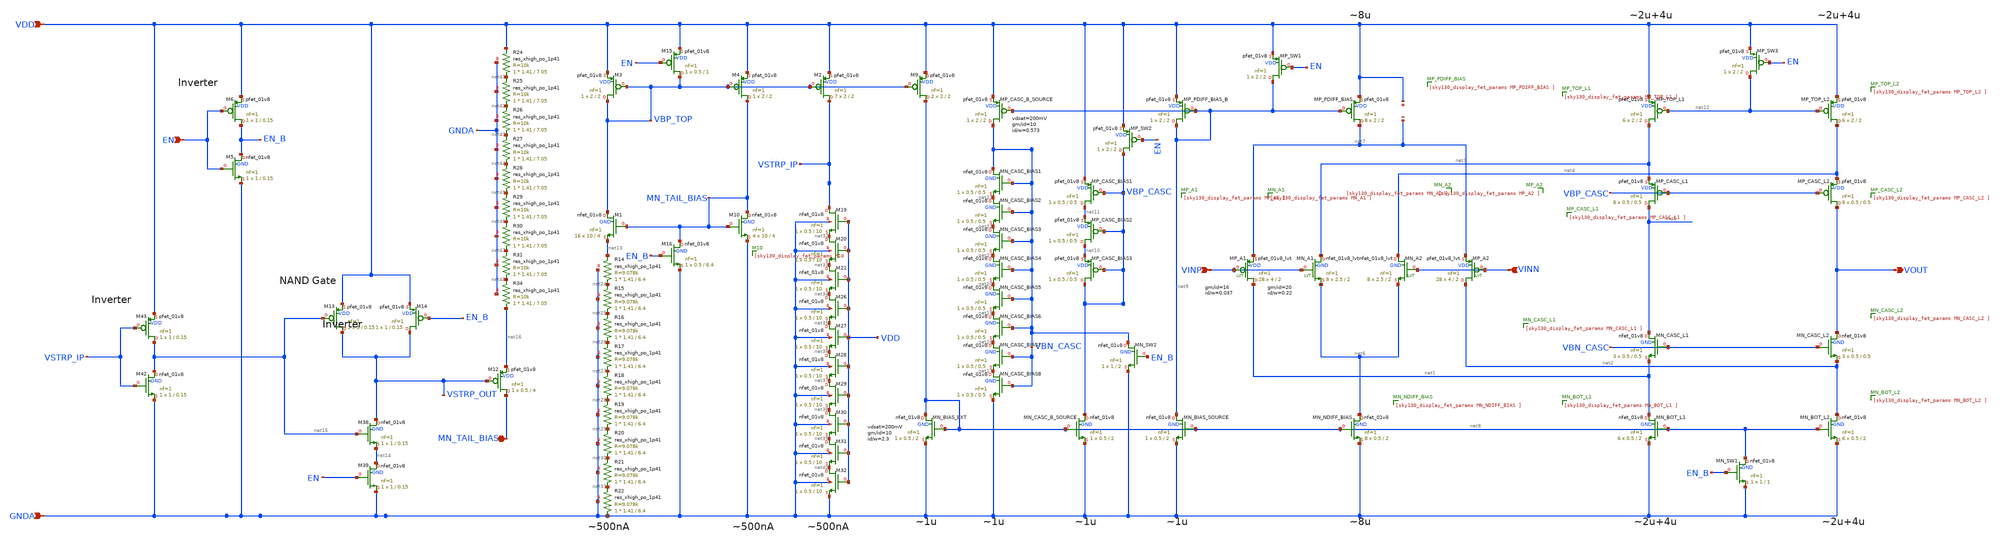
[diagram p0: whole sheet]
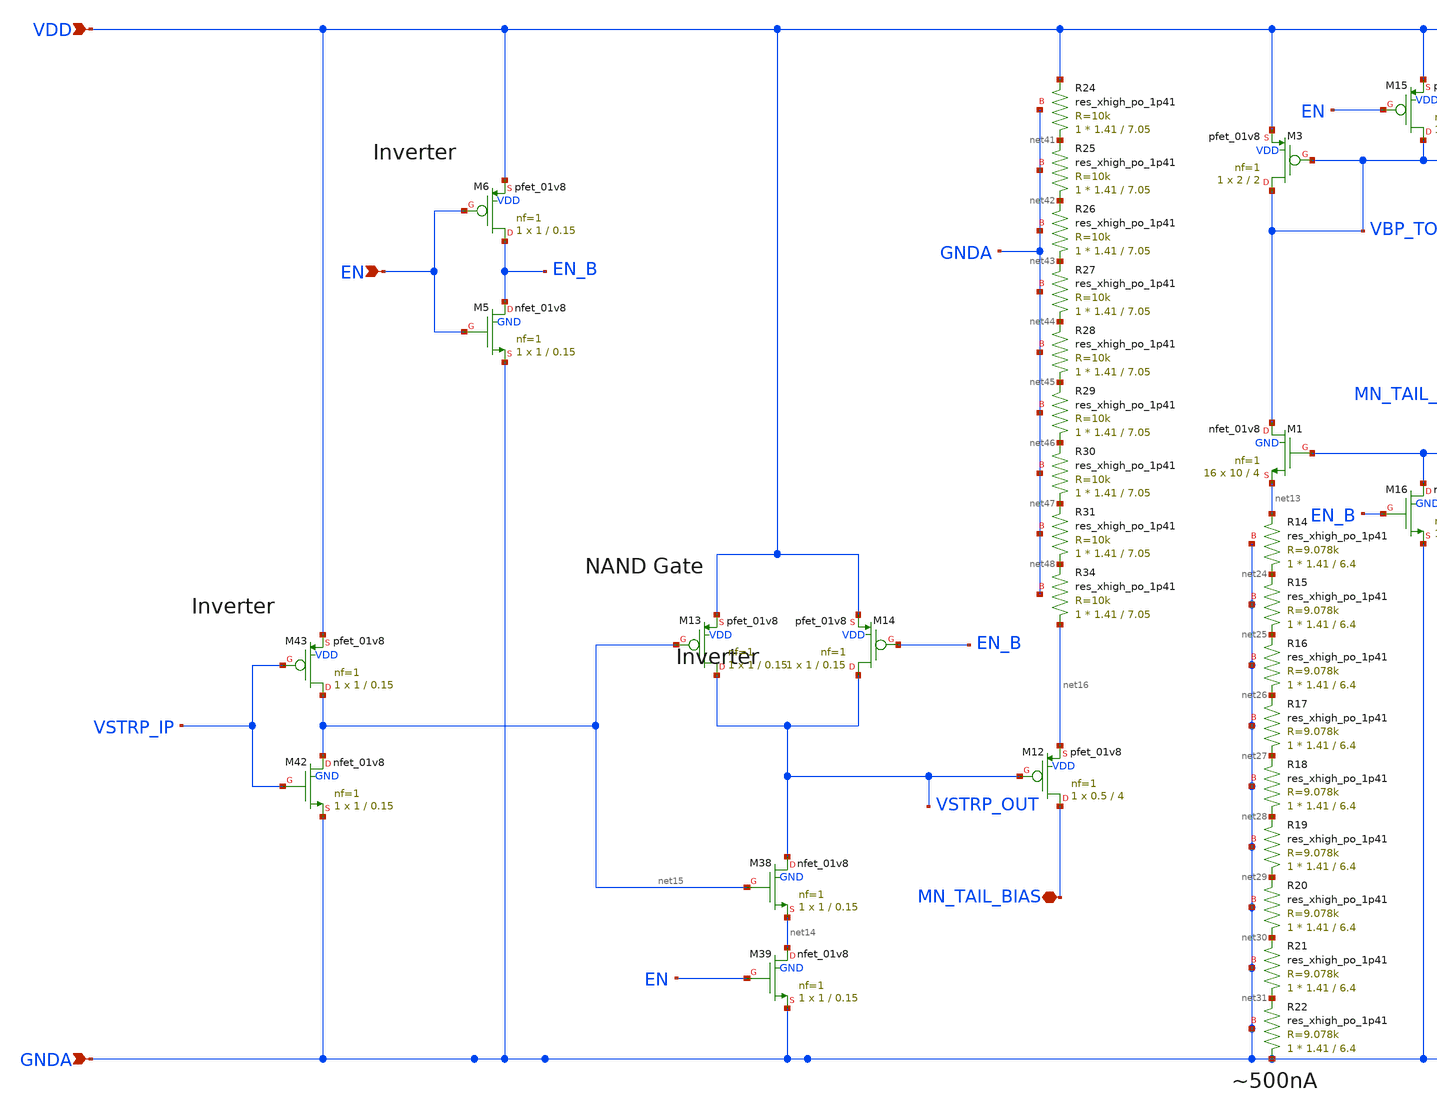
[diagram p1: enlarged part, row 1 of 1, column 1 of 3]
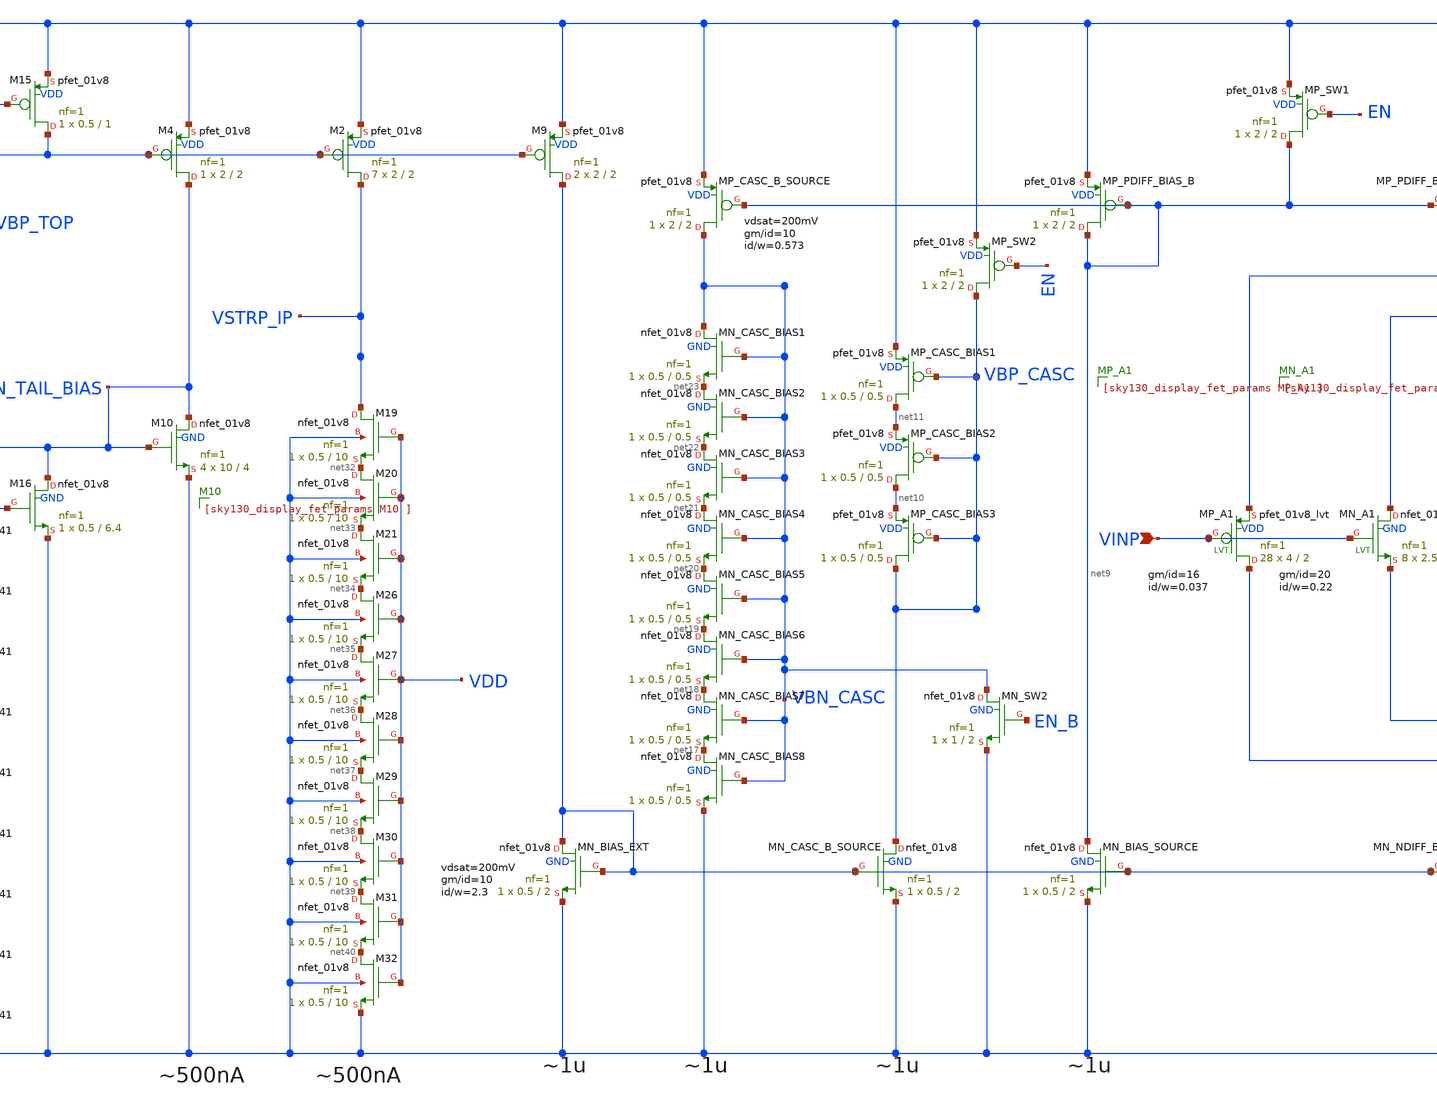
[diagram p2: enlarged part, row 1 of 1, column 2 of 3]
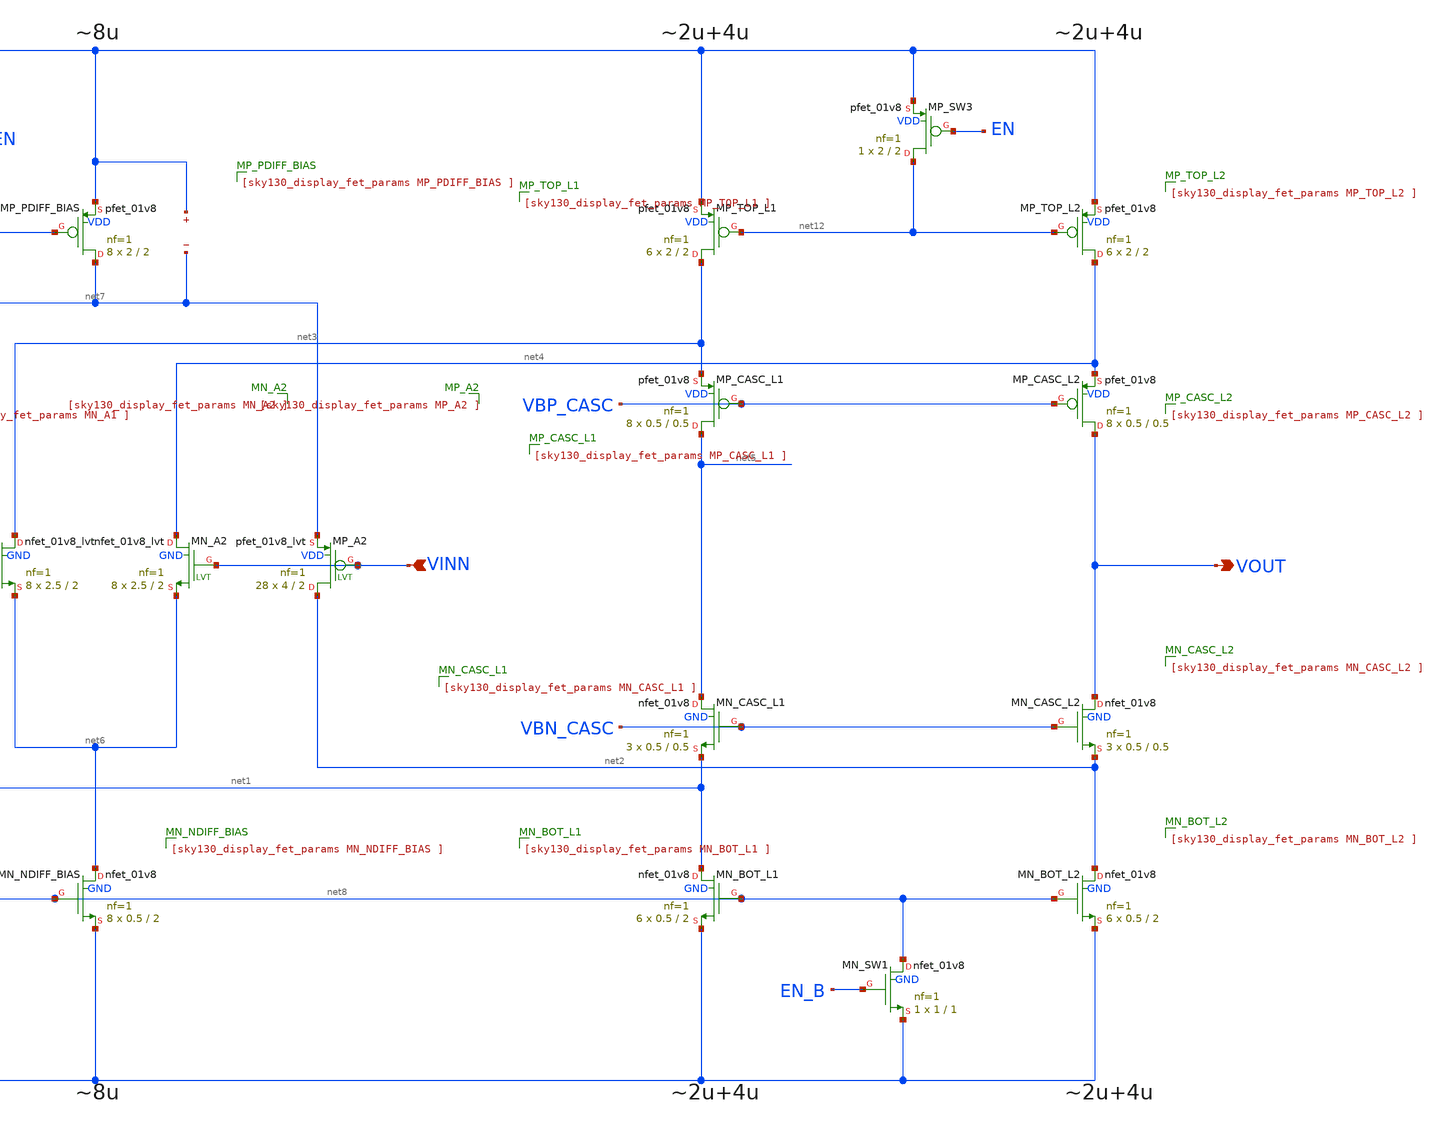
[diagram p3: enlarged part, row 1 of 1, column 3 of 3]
** sch_path: OTAs/Rail_to_Rail_OTA_Inp_IP/fully_differential/Rail_to_Rail_IP_OTA_Fully_Diff_with_Internal_bias.sch
**.subckt Rail_to_Rail_IP_OTA_Fully_Diff_with_Internal_bias VINP VINN VDD GNDA VOUT EN MN_TAIL_BIAS
*.ipin VINP
*.ipin VINN
*.ipin VDD
*.ipin GNDA
*.opin VOUT
*.ipin EN
*.iopin MN_TAIL_BIAS
XMN_BOT_L2 net2 net8 GNDA GND sky130_fd_pr__nfet_01v8 L=2 W=0.5 nf=1 ad='int((1 + 1)/2) * 0.5 / 1 * 0.29'
+ as='int((1 + 2)/2) * 0.5 / 1 * 0.29' pd='2*int((1 + 1)/2) * (0.5 / 1 + 0.29)' ps='2*int((1 + 2)/2) * (0.5 / 1 + 0.29)'
+ nrd='0.29 / 0.5 ' nrs='0.29 / 0.5 ' sa=0 sb=0 sd=0 mult=6 m=6
XMN_CASC_L2 VOUT VBN_CASC net2 GND sky130_fd_pr__nfet_01v8 L=0.5 W=0.5 nf=1 ad='int((1 + 1)/2) * 0.5 / 1 * 0.29'
+ as='int((1 + 2)/2) * 0.5 / 1 * 0.29' pd='2*int((1 + 1)/2) * (0.5 / 1 + 0.29)' ps='2*int((1 + 2)/2) * (0.5 / 1 + 0.29)'
+ nrd='0.29 / 0.5 ' nrs='0.29 / 0.5 ' sa=0 sb=0 sd=0 mult=3 m=3
XMN_BOT_L1 net1 net8 GNDA GND sky130_fd_pr__nfet_01v8 L=2 W=0.5 nf=1 ad='int((1 + 1)/2) * 0.5 / 1 * 0.29'
+ as='int((1 + 2)/2) * 0.5 / 1 * 0.29' pd='2*int((1 + 1)/2) * (0.5 / 1 + 0.29)' ps='2*int((1 + 2)/2) * (0.5 / 1 + 0.29)'
+ nrd='0.29 / 0.5 ' nrs='0.29 / 0.5 ' sa=0 sb=0 sd=0 mult=6 m=6
XMN_CASC_L1 net5 VBN_CASC net1 GND sky130_fd_pr__nfet_01v8 L=0.5 W=0.5 nf=1 ad='int((1 + 1)/2) * 0.5 / 1 * 0.29'
+ as='int((1 + 2)/2) * 0.5 / 1 * 0.29' pd='2*int((1 + 1)/2) * (0.5 / 1 + 0.29)' ps='2*int((1 + 2)/2) * (0.5 / 1 + 0.29)'
+ nrd='0.29 / 0.5 ' nrs='0.29 / 0.5 ' sa=0 sb=0 sd=0 mult=3 m=3
XMP_CASC_L2 VOUT VBP_CASC net4 VDD sky130_fd_pr__pfet_01v8 L=0.5 W=0.5 nf=1 ad='int((1 + 1)/2) * 0.5 / 1 * 0.29'
+ as='int((1 + 2)/2) * 0.5 / 1 * 0.29' pd='2*int((1 + 1)/2) * (0.5 / 1 + 0.29)' ps='2*int((1 + 2)/2) * (0.5 / 1 + 0.29)'
+ nrd='0.29 / 0.5 ' nrs='0.29 / 0.5 ' sa=0 sb=0 sd=0 mult=8 m=8
XMP_CASC_L1 net5 VBP_CASC net3 VDD sky130_fd_pr__pfet_01v8 L=0.5 W=0.5 nf=1 ad='int((1 + 1)/2) * 0.5 / 1 * 0.29'
+ as='int((1 + 2)/2) * 0.5 / 1 * 0.29' pd='2*int((1 + 1)/2) * (0.5 / 1 + 0.29)' ps='2*int((1 + 2)/2) * (0.5 / 1 + 0.29)'
+ nrd='0.29 / 0.5 ' nrs='0.29 / 0.5 ' sa=0 sb=0 sd=0 mult=8 m=8
XMP_TOP_L1 net3 net12 VDD VDD sky130_fd_pr__pfet_01v8 L=2 W=2 nf=1 ad='int((1 + 1)/2) * 2 / 1 * 0.29'
+ as='int((1 + 2)/2) * 2 / 1 * 0.29' pd='2*int((1 + 1)/2) * (2 / 1 + 0.29)' ps='2*int((1 + 2)/2) * (2 / 1 + 0.29)'
+ nrd='0.29 / 2 ' nrs='0.29 / 2 ' sa=0 sb=0 sd=0 mult=6 m=6
XMN_A1 net3 VINP net6 GND sky130_fd_pr__nfet_01v8_lvt L=2 W=2.5 nf=1 ad='int((1 + 1)/2) * 2.5 / 1 * 0.29'
+ as='int((1 + 2)/2) * 2.5 / 1 * 0.29' pd='2*int((1 + 1)/2) * (2.5 / 1 + 0.29)' ps='2*int((1 + 2)/2) * (2.5 / 1 + 0.29)'
+ nrd='0.29 / 2.5 ' nrs='0.29 / 2.5 ' sa=0 sb=0 sd=0 mult=8 m=8
XMN_A2 net4 VINN net6 GND sky130_fd_pr__nfet_01v8_lvt L=2 W=2.5 nf=1 ad='int((1 + 1)/2) * 2.5 / 1 * 0.29'
+ as='int((1 + 2)/2) * 2.5 / 1 * 0.29' pd='2*int((1 + 1)/2) * (2.5 / 1 + 0.29)' ps='2*int((1 + 2)/2) * (2.5 / 1 + 0.29)'
+ nrd='0.29 / 2.5 ' nrs='0.29 / 2.5 ' sa=0 sb=0 sd=0 mult=8 m=8
XMP_A1 net1 VINP net7 VDD sky130_fd_pr__pfet_01v8_lvt L=2 W=4 nf=1 ad='int((1 + 1)/2) * 4 / 1 * 0.29'
+ as='int((1 + 2)/2) * 4 / 1 * 0.29' pd='2*int((1 + 1)/2) * (4 / 1 + 0.29)' ps='2*int((1 + 2)/2) * (4 / 1 + 0.29)'
+ nrd='0.29 / 4 ' nrs='0.29 / 4 ' sa=0 sb=0 sd=0 mult=28 m=28
XMP_A2 net2 VINN net7 VDD sky130_fd_pr__pfet_01v8_lvt L=2 W=4 nf=1 ad='int((1 + 1)/2) * 4 / 1 * 0.29'
+ as='int((1 + 2)/2) * 4 / 1 * 0.29' pd='2*int((1 + 1)/2) * (4 / 1 + 0.29)' ps='2*int((1 + 2)/2) * (4 / 1 + 0.29)'
+ nrd='0.29 / 4 ' nrs='0.29 / 4 ' sa=0 sb=0 sd=0 mult=28 m=28
XMP_PDIFF_BIAS net7 net9 VDD VDD sky130_fd_pr__pfet_01v8 L=2 W=2 nf=1 ad='int((1 + 1)/2) * 2 / 1 * 0.29'
+ as='int((1 + 2)/2) * 2 / 1 * 0.29' pd='2*int((1 + 1)/2) * (2 / 1 + 0.29)' ps='2*int((1 + 2)/2) * (2 / 1 + 0.29)'
+ nrd='0.29 / 2 ' nrs='0.29 / 2 ' sa=0 sb=0 sd=0 mult=8 m=8
XMN_NDIFF_BIAS net6 net8 GNDA GND sky130_fd_pr__nfet_01v8 L=2 W=0.5 nf=1 ad='int((1 + 1)/2) * 0.5 / 1 * 0.29'
+ as='int((1 + 2)/2) * 0.5 / 1 * 0.29' pd='2*int((1 + 1)/2) * (0.5 / 1 + 0.29)' ps='2*int((1 + 2)/2) * (0.5 / 1 + 0.29)'
+ nrd='0.29 / 0.5 ' nrs='0.29 / 0.5 ' sa=0 sb=0 sd=0 mult=8 m=8
XMP_PDIFF_BIAS_B net9 net9 VDD VDD sky130_fd_pr__pfet_01v8 L=2 W=2 nf=1 ad='int((1 + 1)/2) * 2 / 1 * 0.29'
+ as='int((1 + 2)/2) * 2 / 1 * 0.29' pd='2*int((1 + 1)/2) * (2 / 1 + 0.29)' ps='2*int((1 + 2)/2) * (2 / 1 + 0.29)'
+ nrd='0.29 / 2 ' nrs='0.29 / 2 ' sa=0 sb=0 sd=0 mult=1 m=1
XMP_TOP_L2 net4 net12 VDD VDD sky130_fd_pr__pfet_01v8 L=2 W=2 nf=1 ad='int((1 + 1)/2) * 2 / 1 * 0.29'
+ as='int((1 + 2)/2) * 2 / 1 * 0.29' pd='2*int((1 + 1)/2) * (2 / 1 + 0.29)' ps='2*int((1 + 2)/2) * (2 / 1 + 0.29)'
+ nrd='0.29 / 2 ' nrs='0.29 / 2 ' sa=0 sb=0 sd=0 mult=6 m=6
XMN_BIAS_SOURCE net9 net8 GNDA GND sky130_fd_pr__nfet_01v8 L=2 W=0.5 nf=1 ad='int((1 + 1)/2) * 0.5 / 1 * 0.29'
+ as='int((1 + 2)/2) * 0.5 / 1 * 0.29' pd='2*int((1 + 1)/2) * (0.5 / 1 + 0.29)' ps='2*int((1 + 2)/2) * (0.5 / 1 + 0.29)'
+ nrd='0.29 / 0.5 ' nrs='0.29 / 0.5 ' sa=0 sb=0 sd=0 mult=1 m=1
XMN_BIAS_EXT net8 net8 GNDA GND sky130_fd_pr__nfet_01v8 L=2 W=0.5 nf=1 ad='int((1 + 1)/2) * 0.5 / 1 * 0.29'
+ as='int((1 + 2)/2) * 0.5 / 1 * 0.29' pd='2*int((1 + 1)/2) * (0.5 / 1 + 0.29)' ps='2*int((1 + 2)/2) * (0.5 / 1 + 0.29)'
+ nrd='0.29 / 0.5 ' nrs='0.29 / 0.5 ' sa=0 sb=0 sd=0 mult=1 m=1
XMP_CASC_B_SOURCE VBN_CASC net9 VDD VDD sky130_fd_pr__pfet_01v8 L=2 W=2 nf=1 ad='int((1 + 1)/2) * 2 / 1 * 0.29'
+ as='int((1 + 2)/2) * 2 / 1 * 0.29' pd='2*int((1 + 1)/2) * (2 / 1 + 0.29)' ps='2*int((1 + 2)/2) * (2 / 1 + 0.29)'
+ nrd='0.29 / 2 ' nrs='0.29 / 2 ' sa=0 sb=0 sd=0 mult=1 m=1
XMN_CASC_BIAS8 net17 VBN_CASC GNDA GND sky130_fd_pr__nfet_01v8 L=0.5 W=0.5 nf=1 ad='int((1 + 1)/2) * 0.5 / 1 * 0.29'
+ as='int((1 + 2)/2) * 0.5 / 1 * 0.29' pd='2*int((1 + 1)/2) * (0.5 / 1 + 0.29)' ps='2*int((1 + 2)/2) * (0.5 / 1 + 0.29)'
+ nrd='0.29 / 0.5 ' nrs='0.29 / 0.5 ' sa=0 sb=0 sd=0 mult=1 m=1
XMN_CASC_B_SOURCE VBP_CASC net8 GNDA GND sky130_fd_pr__nfet_01v8 L=2 W=0.5 nf=1 ad='int((1 + 1)/2) * 0.5 / 1 * 0.29'
+ as='int((1 + 2)/2) * 0.5 / 1 * 0.29' pd='2*int((1 + 1)/2) * (0.5 / 1 + 0.29)' ps='2*int((1 + 2)/2) * (0.5 / 1 + 0.29)'
+ nrd='0.29 / 0.5 ' nrs='0.29 / 0.5 ' sa=0 sb=0 sd=0 mult=1 m=1
XMP_CASC_BIAS1 net11 VBP_CASC VDD VDD sky130_fd_pr__pfet_01v8 L=0.5 W=0.5 nf=1 ad='int((1 + 1)/2) * 0.5 / 1 * 0.29'
+ as='int((1 + 2)/2) * 0.5 / 1 * 0.29' pd='2*int((1 + 1)/2) * (0.5 / 1 + 0.29)' ps='2*int((1 + 2)/2) * (0.5 / 1 + 0.29)'
+ nrd='0.29 / 0.5 ' nrs='0.29 / 0.5 ' sa=0 sb=0 sd=0 mult=1 m=1
XMN_CASC_BIAS7 net18 VBN_CASC net17 GND sky130_fd_pr__nfet_01v8 L=0.5 W=0.5 nf=1 ad='int((1 + 1)/2) * 0.5 / 1 * 0.29'
+ as='int((1 + 2)/2) * 0.5 / 1 * 0.29' pd='2*int((1 + 1)/2) * (0.5 / 1 + 0.29)' ps='2*int((1 + 2)/2) * (0.5 / 1 + 0.29)'
+ nrd='0.29 / 0.5 ' nrs='0.29 / 0.5 ' sa=0 sb=0 sd=0 mult=1 m=1
XMN_CASC_BIAS6 net19 VBN_CASC net18 GND sky130_fd_pr__nfet_01v8 L=0.5 W=0.5 nf=1 ad='int((1 + 1)/2) * 0.5 / 1 * 0.29'
+ as='int((1 + 2)/2) * 0.5 / 1 * 0.29' pd='2*int((1 + 1)/2) * (0.5 / 1 + 0.29)' ps='2*int((1 + 2)/2) * (0.5 / 1 + 0.29)'
+ nrd='0.29 / 0.5 ' nrs='0.29 / 0.5 ' sa=0 sb=0 sd=0 mult=1 m=1
XMP_CASC_BIAS2 net10 VBP_CASC net11 VDD sky130_fd_pr__pfet_01v8 L=0.5 W=0.5 nf=1 ad='int((1 + 1)/2) * 0.5 / 1 * 0.29'
+ as='int((1 + 2)/2) * 0.5 / 1 * 0.29' pd='2*int((1 + 1)/2) * (0.5 / 1 + 0.29)' ps='2*int((1 + 2)/2) * (0.5 / 1 + 0.29)'
+ nrd='0.29 / 0.5 ' nrs='0.29 / 0.5 ' sa=0 sb=0 sd=0 mult=1 m=1
XMP_CASC_BIAS3 VBP_CASC VBP_CASC net10 VDD sky130_fd_pr__pfet_01v8 L=0.5 W=0.5 nf=1 ad='int((1 + 1)/2) * 0.5 / 1 * 0.29'
+ as='int((1 + 2)/2) * 0.5 / 1 * 0.29' pd='2*int((1 + 1)/2) * (0.5 / 1 + 0.29)' ps='2*int((1 + 2)/2) * (0.5 / 1 + 0.29)'
+ nrd='0.29 / 0.5 ' nrs='0.29 / 0.5 ' sa=0 sb=0 sd=0 mult=1 m=1
XMN_CASC_BIAS5 net20 VBN_CASC net19 GND sky130_fd_pr__nfet_01v8 L=0.5 W=0.5 nf=1 ad='int((1 + 1)/2) * 0.5 / 1 * 0.29'
+ as='int((1 + 2)/2) * 0.5 / 1 * 0.29' pd='2*int((1 + 1)/2) * (0.5 / 1 + 0.29)' ps='2*int((1 + 2)/2) * (0.5 / 1 + 0.29)'
+ nrd='0.29 / 0.5 ' nrs='0.29 / 0.5 ' sa=0 sb=0 sd=0 mult=1 m=1
XMN_CASC_BIAS4 net21 VBN_CASC net20 GND sky130_fd_pr__nfet_01v8 L=0.5 W=0.5 nf=1 ad='int((1 + 1)/2) * 0.5 / 1 * 0.29'
+ as='int((1 + 2)/2) * 0.5 / 1 * 0.29' pd='2*int((1 + 1)/2) * (0.5 / 1 + 0.29)' ps='2*int((1 + 2)/2) * (0.5 / 1 + 0.29)'
+ nrd='0.29 / 0.5 ' nrs='0.29 / 0.5 ' sa=0 sb=0 sd=0 mult=1 m=1
XMN_CASC_BIAS3 net22 VBN_CASC net21 GND sky130_fd_pr__nfet_01v8 L=0.5 W=0.5 nf=1 ad='int((1 + 1)/2) * 0.5 / 1 * 0.29'
+ as='int((1 + 2)/2) * 0.5 / 1 * 0.29' pd='2*int((1 + 1)/2) * (0.5 / 1 + 0.29)' ps='2*int((1 + 2)/2) * (0.5 / 1 + 0.29)'
+ nrd='0.29 / 0.5 ' nrs='0.29 / 0.5 ' sa=0 sb=0 sd=0 mult=1 m=1
XMN_CASC_BIAS1 VBN_CASC VBN_CASC net23 GND sky130_fd_pr__nfet_01v8 L=0.5 W=0.5 nf=1 ad='int((1 + 1)/2) * 0.5 / 1 * 0.29'
+ as='int((1 + 2)/2) * 0.5 / 1 * 0.29' pd='2*int((1 + 1)/2) * (0.5 / 1 + 0.29)' ps='2*int((1 + 2)/2) * (0.5 / 1 + 0.29)'
+ nrd='0.29 / 0.5 ' nrs='0.29 / 0.5 ' sa=0 sb=0 sd=0 mult=1 m=1
XMN_CASC_BIAS2 net23 VBN_CASC net22 GND sky130_fd_pr__nfet_01v8 L=0.5 W=0.5 nf=1 ad='int((1 + 1)/2) * 0.5 / 1 * 0.29'
+ as='int((1 + 2)/2) * 0.5 / 1 * 0.29' pd='2*int((1 + 1)/2) * (0.5 / 1 + 0.29)' ps='2*int((1 + 2)/2) * (0.5 / 1 + 0.29)'
+ nrd='0.29 / 0.5 ' nrs='0.29 / 0.5 ' sa=0 sb=0 sd=0 mult=1 m=1
XMN_SW1 net8 EN_B GNDA GND sky130_fd_pr__nfet_01v8 L=1 W=1 nf=1 ad='int((1 + 1)/2) * 1 / 1 * 0.29' as='int((1 + 2)/2) * 1 / 1 * 0.29'
+ pd='2*int((1 + 1)/2) * (1 / 1 + 0.29)' ps='2*int((1 + 2)/2) * (1 / 1 + 0.29)' nrd='0.29 / 1 ' nrs='0.29 / 1 '
+ sa=0 sb=0 sd=0 mult=1 m=1
XMP_SW1 net9 EN VDD VDD sky130_fd_pr__pfet_01v8 L=2 W=2 nf=1 ad='int((1 + 1)/2) * 2 / 1 * 0.29' as='int((1 + 2)/2) * 2 / 1 * 0.29'
+ pd='2*int((1 + 1)/2) * (2 / 1 + 0.29)' ps='2*int((1 + 2)/2) * (2 / 1 + 0.29)' nrd='0.29 / 2 ' nrs='0.29 / 2 '
+ sa=0 sb=0 sd=0 mult=1 m=1
XMP_SW2 VBP_CASC EN VDD VDD sky130_fd_pr__pfet_01v8 L=2 W=2 nf=1 ad='int((1 + 1)/2) * 2 / 1 * 0.29' as='int((1 + 2)/2) * 2 / 1 * 0.29'
+ pd='2*int((1 + 1)/2) * (2 / 1 + 0.29)' ps='2*int((1 + 2)/2) * (2 / 1 + 0.29)' nrd='0.29 / 2 ' nrs='0.29 / 2 '
+ sa=0 sb=0 sd=0 mult=1 m=1
XMN_SW2 VBN_CASC EN_B GNDA GND sky130_fd_pr__nfet_01v8 L=2 W=1 nf=1 ad='int((1 + 1)/2) * 1 / 1 * 0.29'
+ as='int((1 + 2)/2) * 1 / 1 * 0.29' pd='2*int((1 + 1)/2) * (1 / 1 + 0.29)' ps='2*int((1 + 2)/2) * (1 / 1 + 0.29)'
+ nrd='0.29 / 1 ' nrs='0.29 / 1 ' sa=0 sb=0 sd=0 mult=1 m=1
XMP_SW3 net12 EN VDD VDD sky130_fd_pr__pfet_01v8 L=2 W=2 nf=1 ad='int((1 + 1)/2) * 2 / 1 * 0.29' as='int((1 + 2)/2) * 2 / 1 * 0.29'
+ pd='2*int((1 + 1)/2) * (2 / 1 + 0.29)' ps='2*int((1 + 2)/2) * (2 / 1 + 0.29)' nrd='0.29 / 2 ' nrs='0.29 / 2 '
+ sa=0 sb=0 sd=0 mult=1 m=1
.save v(vdd)
.save v(net7)
XM1 VBP_TOP MN_TAIL_BIAS net13 GND sky130_fd_pr__nfet_01v8 L=4 W=10 nf=1 ad='int((1 + 1)/2) * 10 / 1 * 0.29'
+ as='int((1 + 2)/2) * 10 / 1 * 0.29' pd='2*int((1 + 1)/2) * (10 / 1 + 0.29)' ps='2*int((1 + 2)/2) * (10 / 1 + 0.29)'
+ nrd='0.29 / 10 ' nrs='0.29 / 10 ' sa=0 sb=0 sd=0 mult=16 m=16
XM3 VBP_TOP VBP_TOP VDD VDD sky130_fd_pr__pfet_01v8 L=2 W=2 nf=1 ad='int((1 + 1)/2) * 2 / 1 * 0.29' as='int((1 + 2)/2) * 2 / 1 * 0.29'
+ pd='2*int((1 + 1)/2) * (2 / 1 + 0.29)' ps='2*int((1 + 2)/2) * (2 / 1 + 0.29)' nrd='0.29 / 2 ' nrs='0.29 / 2 '
+ sa=0 sb=0 sd=0 mult=1 m=1
XM4 MN_TAIL_BIAS VBP_TOP VDD VDD sky130_fd_pr__pfet_01v8 L=2 W=2 nf=1 ad='int((1 + 1)/2) * 2 / 1 * 0.29'
+ as='int((1 + 2)/2) * 2 / 1 * 0.29' pd='2*int((1 + 1)/2) * (2 / 1 + 0.29)' ps='2*int((1 + 2)/2) * (2 / 1 + 0.29)'
+ nrd='0.29 / 2 ' nrs='0.29 / 2 ' sa=0 sb=0 sd=0 mult=1 m=1
XM10 MN_TAIL_BIAS MN_TAIL_BIAS GNDA GND sky130_fd_pr__nfet_01v8 L=4 W=10 nf=1 ad='int((1 + 1)/2) * 10 / 1 * 0.29'
+ as='int((1 + 2)/2) * 10 / 1 * 0.29' pd='2*int((1 + 1)/2) * (10 / 1 + 0.29)' ps='2*int((1 + 2)/2) * (10 / 1 + 0.29)'
+ nrd='0.29 / 10 ' nrs='0.29 / 10 ' sa=0 sb=0 sd=0 mult=4 m=4
XM16 MN_TAIL_BIAS EN_B GNDA GND sky130_fd_pr__nfet_01v8 L=6.4 W=0.5 nf=1 ad='int((1 + 1)/2) * 0.5 / 1 * 0.29'
+ as='int((1 + 2)/2) * 0.5 / 1 * 0.29' pd='2*int((1 + 1)/2) * (0.5 / 1 + 0.29)' ps='2*int((1 + 2)/2) * (0.5 / 1 + 0.29)'
+ nrd='0.29 / 0.5 ' nrs='0.29 / 0.5 ' sa=0 sb=0 sd=0 mult=1 m=1
XR14 net24 net13 GNDA sky130_fd_pr__res_xhigh_po_1p41 L=6.4 mult=1 m=1
XR15 net25 net24 GNDA sky130_fd_pr__res_xhigh_po_1p41 L=6.4 mult=1 m=1
XR16 net26 net25 GNDA sky130_fd_pr__res_xhigh_po_1p41 L=6.4 mult=1 m=1
XR17 net27 net26 GNDA sky130_fd_pr__res_xhigh_po_1p41 L=6.4 mult=1 m=1
XR18 net28 net27 GNDA sky130_fd_pr__res_xhigh_po_1p41 L=6.4 mult=1 m=1
XR19 net29 net28 GNDA sky130_fd_pr__res_xhigh_po_1p41 L=6.4 mult=1 m=1
XR20 net30 net29 GNDA sky130_fd_pr__res_xhigh_po_1p41 L=6.4 mult=1 m=1
XR21 net31 net30 GNDA sky130_fd_pr__res_xhigh_po_1p41 L=6.4 mult=1 m=1
XR22 GNDA net31 GNDA sky130_fd_pr__res_xhigh_po_1p41 L=6.4 mult=1 m=1
XM15 VBP_TOP EN VDD VDD sky130_fd_pr__pfet_01v8 L=1 W=0.5 nf=1 ad='int((1 + 1)/2) * 0.5 / 1 * 0.29' as='int((1 + 2)/2) * 0.5 / 1 * 0.29'
+ pd='2*int((1 + 1)/2) * (0.5 / 1 + 0.29)' ps='2*int((1 + 2)/2) * (0.5 / 1 + 0.29)' nrd='0.29 / 0.5 ' nrs='0.29 / 0.5 '
+ sa=0 sb=0 sd=0 mult=1 m=1
XM2 VSTRP_IP VBP_TOP VDD VDD sky130_fd_pr__pfet_01v8 L=2 W=2 nf=1 ad='int((1 + 1)/2) * 2 / 1 * 0.29'
+ as='int((1 + 2)/2) * 2 / 1 * 0.29' pd='2*int((1 + 1)/2) * (2 / 1 + 0.29)' ps='2*int((1 + 2)/2) * (2 / 1 + 0.29)'
+ nrd='0.29 / 2 ' nrs='0.29 / 2 ' sa=0 sb=0 sd=0 mult=7 m=7
XM19 VSTRP_IP VDD net32 GNDA sky130_fd_pr__nfet_01v8 L=10 W=0.5 nf=1 ad='int((1 + 1)/2) * 0.5 / 1 * 0.29'
+ as='int((1 + 2)/2) * 0.5 / 1 * 0.29' pd='2*int((1 + 1)/2) * (0.5 / 1 + 0.29)' ps='2*int((1 + 2)/2) * (0.5 / 1 + 0.29)'
+ nrd='0.29 / 0.5 ' nrs='0.29 / 0.5 ' sa=0 sb=0 sd=0 mult=1 m=1
XM20 net32 VDD net33 GNDA sky130_fd_pr__nfet_01v8 L=10 W=0.5 nf=1 ad='int((1 + 1)/2) * 0.5 / 1 * 0.29'
+ as='int((1 + 2)/2) * 0.5 / 1 * 0.29' pd='2*int((1 + 1)/2) * (0.5 / 1 + 0.29)' ps='2*int((1 + 2)/2) * (0.5 / 1 + 0.29)'
+ nrd='0.29 / 0.5 ' nrs='0.29 / 0.5 ' sa=0 sb=0 sd=0 mult=1 m=1
XM21 net33 VDD net34 GNDA sky130_fd_pr__nfet_01v8 L=10 W=0.5 nf=1 ad='int((1 + 1)/2) * 0.5 / 1 * 0.29'
+ as='int((1 + 2)/2) * 0.5 / 1 * 0.29' pd='2*int((1 + 1)/2) * (0.5 / 1 + 0.29)' ps='2*int((1 + 2)/2) * (0.5 / 1 + 0.29)'
+ nrd='0.29 / 0.5 ' nrs='0.29 / 0.5 ' sa=0 sb=0 sd=0 mult=1 m=1
XM26 net34 VDD net35 GNDA sky130_fd_pr__nfet_01v8 L=10 W=0.5 nf=1 ad='int((1 + 1)/2) * 0.5 / 1 * 0.29'
+ as='int((1 + 2)/2) * 0.5 / 1 * 0.29' pd='2*int((1 + 1)/2) * (0.5 / 1 + 0.29)' ps='2*int((1 + 2)/2) * (0.5 / 1 + 0.29)'
+ nrd='0.29 / 0.5 ' nrs='0.29 / 0.5 ' sa=0 sb=0 sd=0 mult=1 m=1
XM27 net35 VDD net36 GNDA sky130_fd_pr__nfet_01v8 L=10 W=0.5 nf=1 ad='int((1 + 1)/2) * 0.5 / 1 * 0.29'
+ as='int((1 + 2)/2) * 0.5 / 1 * 0.29' pd='2*int((1 + 1)/2) * (0.5 / 1 + 0.29)' ps='2*int((1 + 2)/2) * (0.5 / 1 + 0.29)'
+ nrd='0.29 / 0.5 ' nrs='0.29 / 0.5 ' sa=0 sb=0 sd=0 mult=1 m=1
XM28 net36 VDD net37 GNDA sky130_fd_pr__nfet_01v8 L=10 W=0.5 nf=1 ad='int((1 + 1)/2) * 0.5 / 1 * 0.29'
+ as='int((1 + 2)/2) * 0.5 / 1 * 0.29' pd='2*int((1 + 1)/2) * (0.5 / 1 + 0.29)' ps='2*int((1 + 2)/2) * (0.5 / 1 + 0.29)'
+ nrd='0.29 / 0.5 ' nrs='0.29 / 0.5 ' sa=0 sb=0 sd=0 mult=1 m=1
XM29 net37 VDD net38 GNDA sky130_fd_pr__nfet_01v8 L=10 W=0.5 nf=1 ad='int((1 + 1)/2) * 0.5 / 1 * 0.29'
+ as='int((1 + 2)/2) * 0.5 / 1 * 0.29' pd='2*int((1 + 1)/2) * (0.5 / 1 + 0.29)' ps='2*int((1 + 2)/2) * (0.5 / 1 + 0.29)'
+ nrd='0.29 / 0.5 ' nrs='0.29 / 0.5 ' sa=0 sb=0 sd=0 mult=1 m=1
XM30 net38 VDD net39 GNDA sky130_fd_pr__nfet_01v8 L=10 W=0.5 nf=1 ad='int((1 + 1)/2) * 0.5 / 1 * 0.29'
+ as='int((1 + 2)/2) * 0.5 / 1 * 0.29' pd='2*int((1 + 1)/2) * (0.5 / 1 + 0.29)' ps='2*int((1 + 2)/2) * (0.5 / 1 + 0.29)'
+ nrd='0.29 / 0.5 ' nrs='0.29 / 0.5 ' sa=0 sb=0 sd=0 mult=1 m=1
XM31 net39 VDD net40 GNDA sky130_fd_pr__nfet_01v8 L=10 W=0.5 nf=1 ad='int((1 + 1)/2) * 0.5 / 1 * 0.29'
+ as='int((1 + 2)/2) * 0.5 / 1 * 0.29' pd='2*int((1 + 1)/2) * (0.5 / 1 + 0.29)' ps='2*int((1 + 2)/2) * (0.5 / 1 + 0.29)'
+ nrd='0.29 / 0.5 ' nrs='0.29 / 0.5 ' sa=0 sb=0 sd=0 mult=1 m=1
XM32 net40 VDD GNDA GNDA sky130_fd_pr__nfet_01v8 L=10 W=0.5 nf=1 ad='int((1 + 1)/2) * 0.5 / 1 * 0.29'
+ as='int((1 + 2)/2) * 0.5 / 1 * 0.29' pd='2*int((1 + 1)/2) * (0.5 / 1 + 0.29)' ps='2*int((1 + 2)/2) * (0.5 / 1 + 0.29)'
+ nrd='0.29 / 0.5 ' nrs='0.29 / 0.5 ' sa=0 sb=0 sd=0 mult=1 m=1
XM12 MN_TAIL_BIAS VSTRP_OUT net16 VDD sky130_fd_pr__pfet_01v8 L=4 W=0.5 nf=1 ad='int((1 + 1)/2) * 0.5 / 1 * 0.29'
+ as='int((1 + 2)/2) * 0.5 / 1 * 0.29' pd='2*int((1 + 1)/2) * (0.5 / 1 + 0.29)' ps='2*int((1 + 2)/2) * (0.5 / 1 + 0.29)'
+ nrd='0.29 / 0.5 ' nrs='0.29 / 0.5 ' sa=0 sb=0 sd=0 mult=1 m=1
XR24 net41 VDD GNDA sky130_fd_pr__res_xhigh_po_1p41 L=7.05 mult=1 m=1
XR25 net42 net41 GNDA sky130_fd_pr__res_xhigh_po_1p41 L=7.05 mult=1 m=1
XR26 net43 net42 GNDA sky130_fd_pr__res_xhigh_po_1p41 L=7.05 mult=1 m=1
XR27 net44 net43 GNDA sky130_fd_pr__res_xhigh_po_1p41 L=7.05 mult=1 m=1
XR28 net45 net44 GNDA sky130_fd_pr__res_xhigh_po_1p41 L=7.05 mult=1 m=1
XR29 net46 net45 GNDA sky130_fd_pr__res_xhigh_po_1p41 L=7.05 mult=1 m=1
XR30 net47 net46 GNDA sky130_fd_pr__res_xhigh_po_1p41 L=7.05 mult=1 m=1
XR31 net48 net47 GNDA sky130_fd_pr__res_xhigh_po_1p41 L=7.05 mult=1 m=1
XR34 net16 net48 GNDA sky130_fd_pr__res_xhigh_po_1p41 L=7.05 mult=1 m=1
XM5 EN_B EN GNDA GND sky130_fd_pr__nfet_01v8 L=0.15 W=1 nf=1 ad='int((1 + 1)/2) * 1 / 1 * 0.29' as='int((1 + 2)/2) * 1 / 1 * 0.29'
+ pd='2*int((1 + 1)/2) * (1 / 1 + 0.29)' ps='2*int((1 + 2)/2) * (1 / 1 + 0.29)' nrd='0.29 / 1 ' nrs='0.29 / 1 '
+ sa=0 sb=0 sd=0 mult=1 m=1
XM6 EN_B EN VDD VDD sky130_fd_pr__pfet_01v8 L=0.15 W=1 nf=1 ad='int((1 + 1)/2) * 1 / 1 * 0.29' as='int((1 + 2)/2) * 1 / 1 * 0.29'
+ pd='2*int((1 + 1)/2) * (1 / 1 + 0.29)' ps='2*int((1 + 2)/2) * (1 / 1 + 0.29)' nrd='0.29 / 1 ' nrs='0.29 / 1 '
+ sa=0 sb=0 sd=0 mult=1 m=1
XM38 VSTRP_OUT net15 net14 GND sky130_fd_pr__nfet_01v8 L=0.15 W=1 nf=1 ad='int((1 + 1)/2) * 1 / 1 * 0.29'
+ as='int((1 + 2)/2) * 1 / 1 * 0.29' pd='2*int((1 + 1)/2) * (1 / 1 + 0.29)' ps='2*int((1 + 2)/2) * (1 / 1 + 0.29)'
+ nrd='0.29 / 1 ' nrs='0.29 / 1 ' sa=0 sb=0 sd=0 mult=1 m=1
XM39 net14 EN GNDA GND sky130_fd_pr__nfet_01v8 L=0.15 W=1 nf=1 ad='int((1 + 1)/2) * 1 / 1 * 0.29' as='int((1 + 2)/2) * 1 / 1 * 0.29'
+ pd='2*int((1 + 1)/2) * (1 / 1 + 0.29)' ps='2*int((1 + 2)/2) * (1 / 1 + 0.29)' nrd='0.29 / 1 ' nrs='0.29 / 1 '
+ sa=0 sb=0 sd=0 mult=1 m=1
XM42 net15 VSTRP_IP GNDA GND sky130_fd_pr__nfet_01v8 L=0.15 W=1 nf=1 ad='int((1 + 1)/2) * 1 / 1 * 0.29'
+ as='int((1 + 2)/2) * 1 / 1 * 0.29' pd='2*int((1 + 1)/2) * (1 / 1 + 0.29)' ps='2*int((1 + 2)/2) * (1 / 1 + 0.29)'
+ nrd='0.29 / 1 ' nrs='0.29 / 1 ' sa=0 sb=0 sd=0 mult=1 m=1
XM43 net15 VSTRP_IP VDD VDD sky130_fd_pr__pfet_01v8 L=0.15 W=1 nf=1 ad='int((1 + 1)/2) * 1 / 1 * 0.29'
+ as='int((1 + 2)/2) * 1 / 1 * 0.29' pd='2*int((1 + 1)/2) * (1 / 1 + 0.29)' ps='2*int((1 + 2)/2) * (1 / 1 + 0.29)'
+ nrd='0.29 / 1 ' nrs='0.29 / 1 ' sa=0 sb=0 sd=0 mult=1 m=1
XM13 VSTRP_OUT net15 VDD VDD sky130_fd_pr__pfet_01v8 L=0.15 W=1 nf=1 ad='int((1 + 1)/2) * 1 / 1 * 0.29'
+ as='int((1 + 2)/2) * 1 / 1 * 0.29' pd='2*int((1 + 1)/2) * (1 / 1 + 0.29)' ps='2*int((1 + 2)/2) * (1 / 1 + 0.29)'
+ nrd='0.29 / 1 ' nrs='0.29 / 1 ' sa=0 sb=0 sd=0 mult=1 m=1
XM14 VSTRP_OUT EN_B VDD VDD sky130_fd_pr__pfet_01v8 L=0.15 W=1 nf=1 ad='int((1 + 1)/2) * 1 / 1 * 0.29'
+ as='int((1 + 2)/2) * 1 / 1 * 0.29' pd='2*int((1 + 1)/2) * (1 / 1 + 0.29)' ps='2*int((1 + 2)/2) * (1 / 1 + 0.29)'
+ nrd='0.29 / 1 ' nrs='0.29 / 1 ' sa=0 sb=0 sd=0 mult=1 m=1
XM9 net8 VBP_TOP VDD VDD sky130_fd_pr__pfet_01v8 L=2 W=2 nf=1 ad='int((1 + 1)/2) * 2 / 1 * 0.29' as='int((1 + 2)/2) * 2 / 1 * 0.29'
+ pd='2*int((1 + 1)/2) * (2 / 1 + 0.29)' ps='2*int((1 + 2)/2) * (2 / 1 + 0.29)' nrd='0.29 / 2 ' nrs='0.29 / 2 '
+ sa=0 sb=0 sd=0 mult=2 m=2
**.ends
.end
